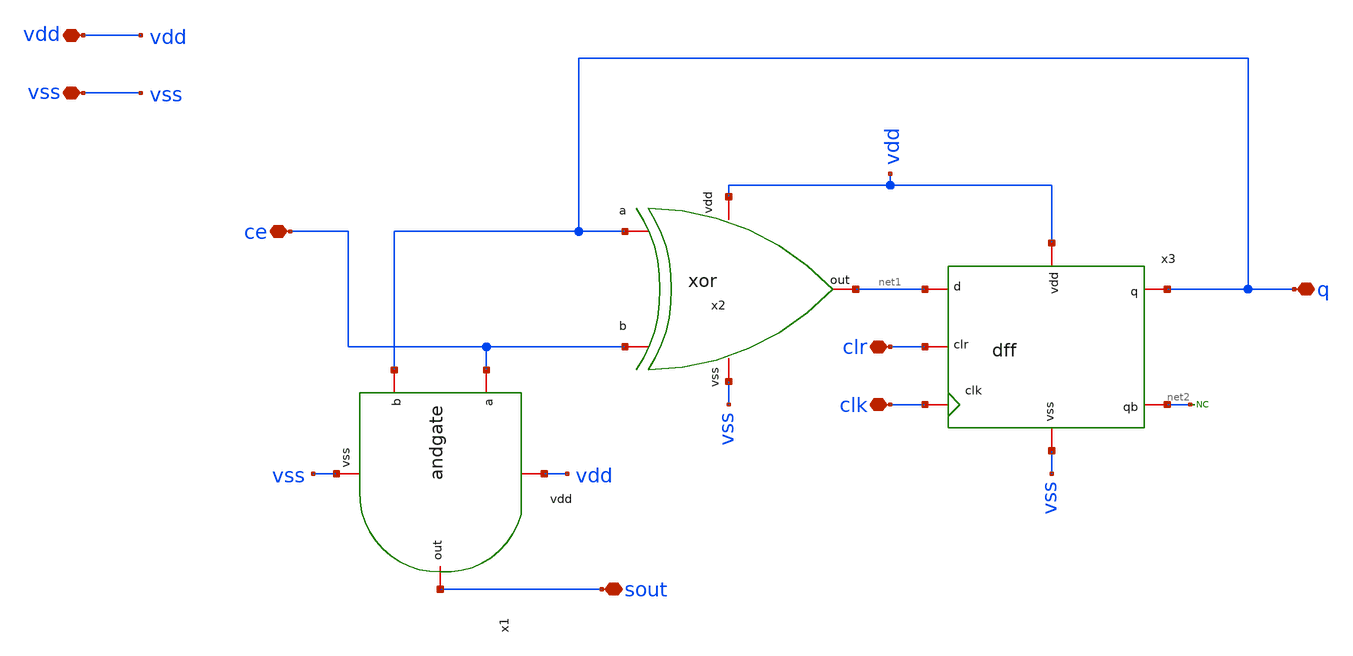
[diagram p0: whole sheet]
** sch_path: design/blocks/count1bit/schematic/count1bit.sch
**.subckt count1bit ce clk clr sout q vdd vss
*.iopin ce
*.iopin clk
*.iopin clr
*.iopin sout
*.iopin q
*.iopin vdd
*.iopin vss
x1 vdd ce sout q vss andgate
x2 vdd q net1 ce vss xor
x3 q net2 net1 vss clk clr vdd dff
* noconn #net2
**.ends
.end
